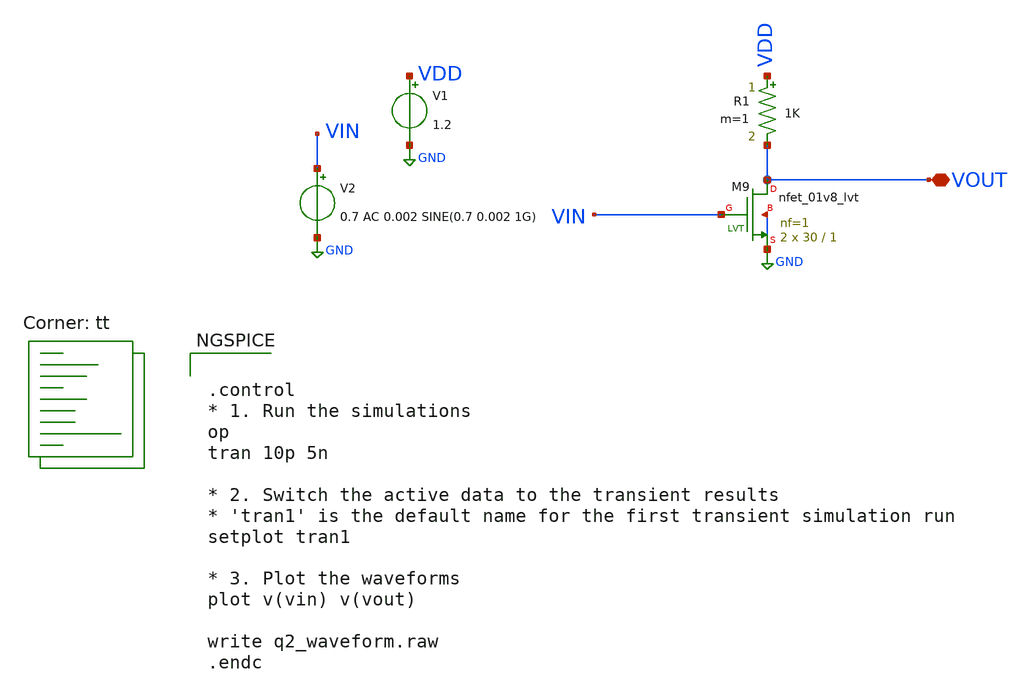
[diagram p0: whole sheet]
** sch_path: cs_amplifier.sch
**.subckt cs_amplifier VOUT
*.iopin VOUT
XM9 VOUT VIN GND GND sky130_fd_pr__nfet_01v8_lvt L=1 W=30 nf=1 ad='int((nf+1)/2) * W/nf * 0.29' as='int((nf+2)/2) * W/nf * 0.29'
+ pd='2*int((nf+1)/2) * (W/nf + 0.29)' ps='2*int((nf+2)/2) * (W/nf + 0.29)' nrd='0.29 / W' nrs='0.29 / W'
+ sa=0 sb=0 sd=0 mult=2 m=2
V1 VDD GND 1.2
V2 VIN GND 0.7 AC 0.002 SINE(0.7 0.002 1G)
R1 VDD VOUT 1K m=1
**** begin user architecture code


.control
* 1. Run the simulations
op
tran 10p 5n

* 2. Switch the active data to the transient results
* 'tran1' is the default name for the first transient simulation run
setplot tran1

* 3. Plot the waveforms
plot v(vin) v(vout)

write q2_waveform.raw
.endc

.lib $::SKYWATER_MODELS/sky130.lib.spice tt
**** end user architecture code
**.ends
.GLOBAL GND
.end
